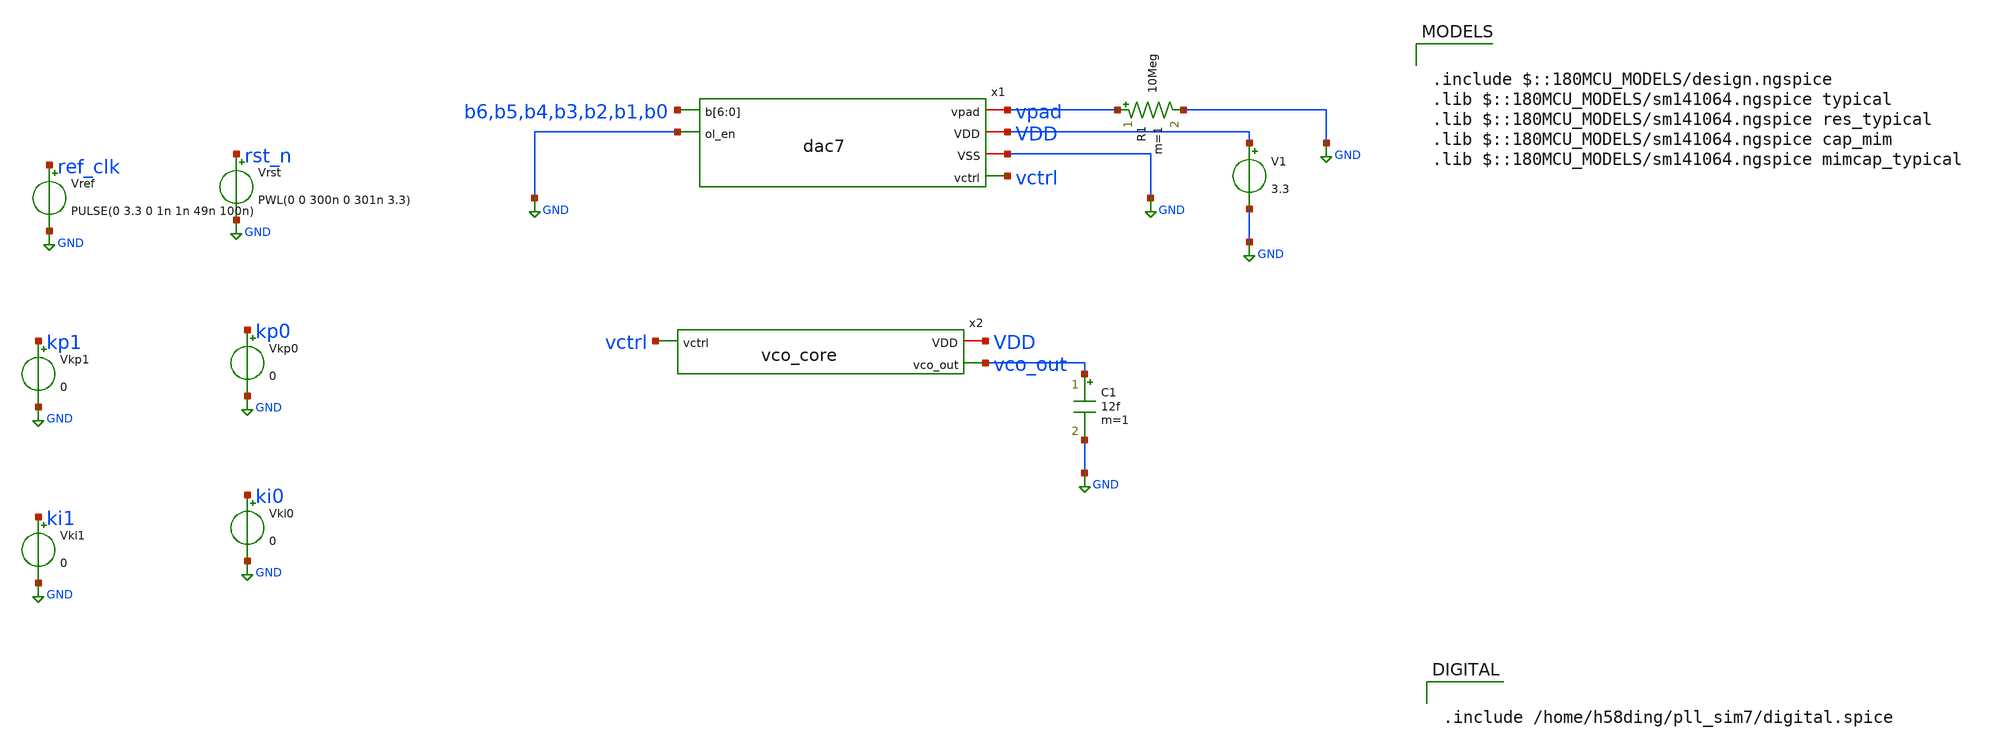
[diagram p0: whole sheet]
** sch_path: xschem/pll_dac/tb_pll7.sch
**.subckt tb_pll7
V1 VDD GND 3.3
R1 vpad GND 10Meg m=1
Vrst rst_n GND PWL(0 0 300n 0 301n 3.3)
Vref ref_clk GND PULSE(0 3.3 0 1n 1n 49n 100n)
Vkp0 kp0 GND 0
Vkp1 kp1 GND 0
Vki0 ki0 GND 0
Vki1 ki1 GND 0
x2 VDD vctrl vco_out vco_core
C1 vco_out GND 12f m=1
x1 b6 b5 b4 b3 b2 b1 b0 GND vpad VDD GND vctrl dac7
**** begin user architecture code

.include $::180MCU_MODELS/design.ngspice
.lib $::180MCU_MODELS/sm141064.ngspice typical
.lib $::180MCU_MODELS/sm141064.ngspice res_typical
.lib $::180MCU_MODELS/sm141064.ngspice cap_mim
.lib $::180MCU_MODELS/sm141064.ngspice mimcap_typical



.ic v(x2.n0)=0 v(x2.n1)=3.3 v(x2.n2)=0 v(x2.n3)=3.3 v(x2.n4)=0
.control
save v(vco_out) v(vctrl)
tran 0.1n 40u 10u
plot v(vctrl)
linearize v(vco_out)
set specwindow=hanning
fft v(vco_out)
let mag = db(mag(v(vco_out)))
meas sp f_peak max_at mag from=60e6 to=100e6
meas sp peak max mag from=60e6 to=100e6
meas sp spur_low max mag from=75e6 to=79e6
meas sp spur_high max mag from=81e6 to=85e6
let dbc_low = spur_low - peak
let dbc_high = spur_high - peak
print dbc_low dbc_high
plot mag xlimit 70e6 90e6 title VCO_spectrum
.endc




.include /home/h58ding/pll_sim7/digital.spice


**** end user architecture code
**.ends
.GLOBAL GND
.end
